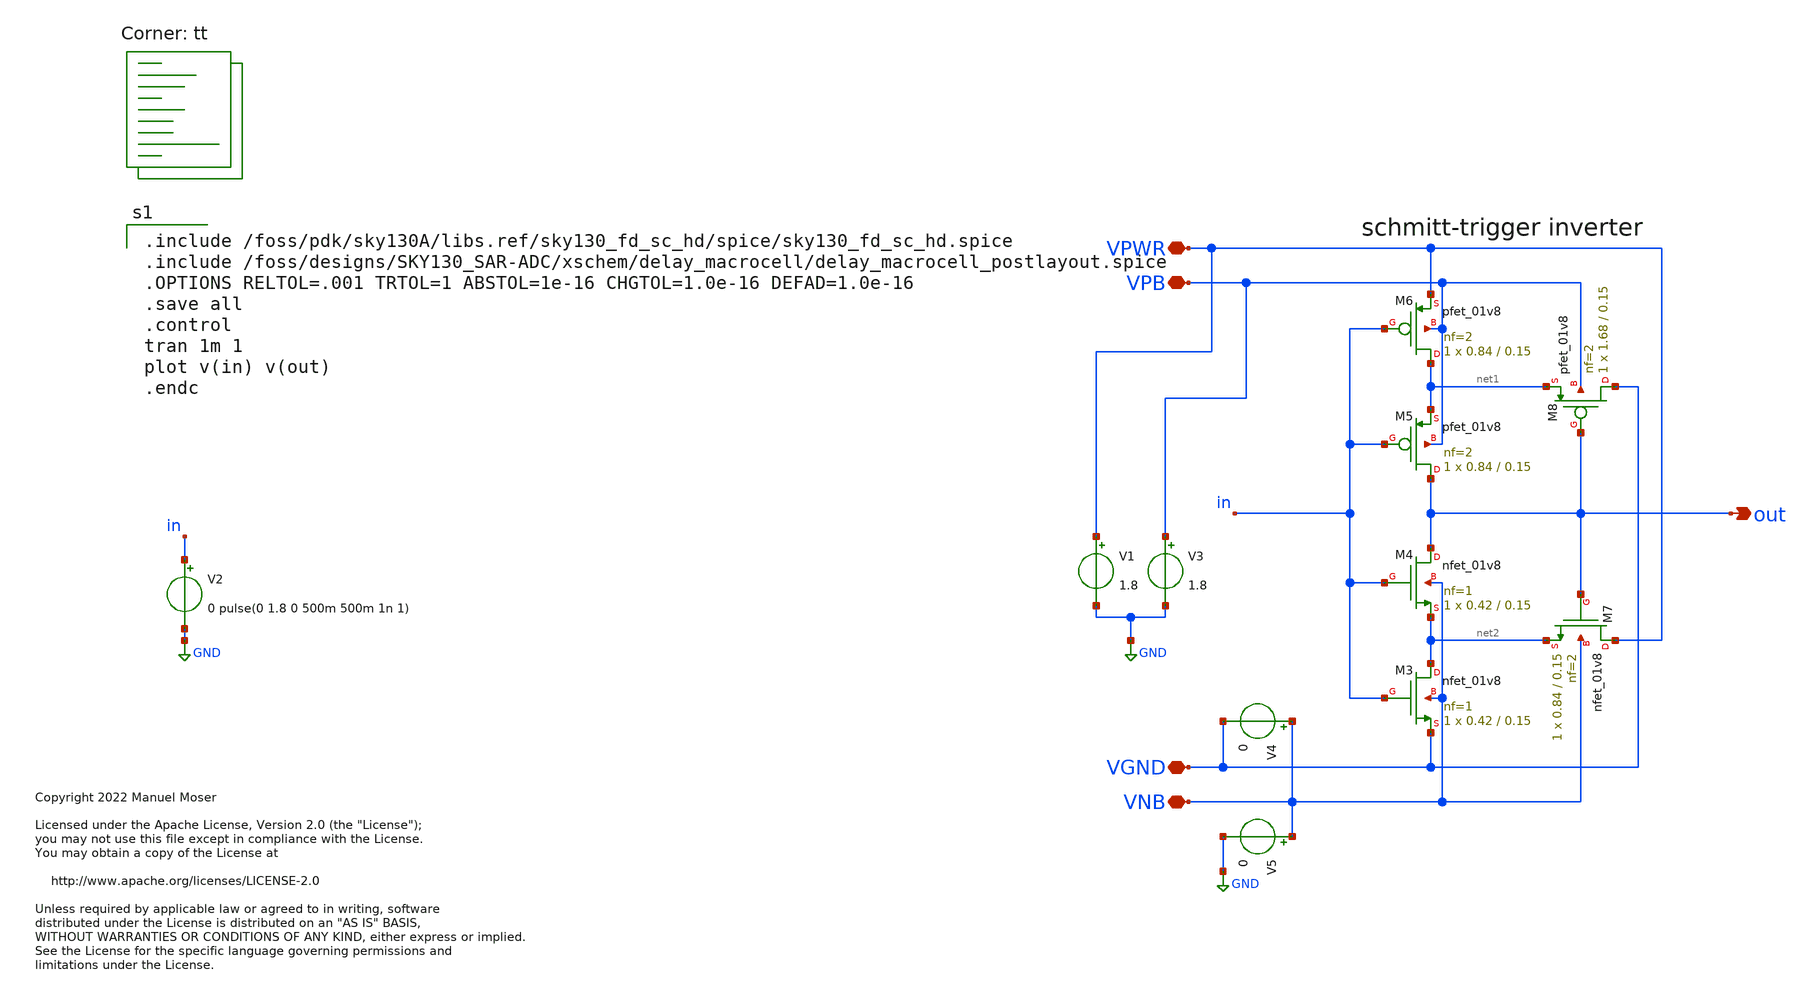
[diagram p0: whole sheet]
** sch_path: xschem/sky130_mm_sc_hd_dly5ns/schmitttrigger.sch
* Copyright 2022 Manuel Moser
* Licensed under the Apache License, Version 2.0 (the "License");
**.subckt schmitttrigger VPWR VGND out VPB VNB
*.iopin VPWR
*.iopin VGND
*.opin out
*.iopin VPB
*.iopin VNB
V1 VPWR GND 1.8
V2 in GND 0 pulse(0 1.8 0 500m 500m 1n 1)
XM3 net2 in VGND VNB sky130_fd_pr__nfet_01v8 L=0.15 W=0.42 nf=1 ad='int((nf+1)/2) * W/nf * 0.29' as='int((nf+2)/2) * W/nf * 0.29'
+ pd='2*int((nf+1)/2) * (W/nf + 0.29)' ps='2*int((nf+2)/2) * (W/nf + 0.29)' nrd='0.29 / W' nrs='0.29 / W'
+ sa=0 sb=0 sd=0 mult=1 m=1
XM4 out in net2 VNB sky130_fd_pr__nfet_01v8 L=0.15 W=0.42 nf=1 ad='int((nf+1)/2) * W/nf * 0.29' as='int((nf+2)/2) * W/nf * 0.29'
+ pd='2*int((nf+1)/2) * (W/nf + 0.29)' ps='2*int((nf+2)/2) * (W/nf + 0.29)' nrd='0.29 / W' nrs='0.29 / W'
+ sa=0 sb=0 sd=0 mult=1 m=1
XM5 out in net1 VPB sky130_fd_pr__pfet_01v8 L=0.15 W=0.84 nf=2 ad='int((nf+1)/2) * W/nf * 0.29' as='int((nf+2)/2) * W/nf * 0.29'
+ pd='2*int((nf+1)/2) * (W/nf + 0.29)' ps='2*int((nf+2)/2) * (W/nf + 0.29)' nrd='0.29 / W' nrs='0.29 / W'
+ sa=0 sb=0 sd=0 mult=1 m=1
XM6 net1 in VPWR VPB sky130_fd_pr__pfet_01v8 L=0.15 W=0.84 nf=2 ad='int((nf+1)/2) * W/nf * 0.29' as='int((nf+2)/2) * W/nf * 0.29'
+ pd='2*int((nf+1)/2) * (W/nf + 0.29)' ps='2*int((nf+2)/2) * (W/nf + 0.29)' nrd='0.29 / W' nrs='0.29 / W'
+ sa=0 sb=0 sd=0 mult=1 m=1
XM7 VPWR out net2 VNB sky130_fd_pr__nfet_01v8 L=0.15 W=0.84 nf=2 ad='int((nf+1)/2) * W/nf * 0.29' as='int((nf+2)/2) * W/nf * 0.29'
+ pd='2*int((nf+1)/2) * (W/nf + 0.29)' ps='2*int((nf+2)/2) * (W/nf + 0.29)' nrd='0.29 / W' nrs='0.29 / W'
+ sa=0 sb=0 sd=0 mult=1 m=1
XM8 VGND out net1 VPB sky130_fd_pr__pfet_01v8 L=0.15 W=1.68 nf=2 ad='int((nf+1)/2) * W/nf * 0.29' as='int((nf+2)/2) * W/nf * 0.29'
+ pd='2*int((nf+1)/2) * (W/nf + 0.29)' ps='2*int((nf+2)/2) * (W/nf + 0.29)' nrd='0.29 / W' nrs='0.29 / W'
+ sa=0 sb=0 sd=0 mult=1 m=1
V3 VPB GND 1.8
V4 VNB VGND 0
V5 VNB GND 0
**** begin user architecture code

.include /foss/pdk/sky130A/libs.ref/sky130_fd_sc_hd/spice/sky130_fd_sc_hd.spice
.include /foss/designs/SKY130_SAR-ADC/xschem/delay_macrocell/delay_macrocell_postlayout.spice
.OPTIONS RELTOL=.001 TRTOL=1 ABSTOL=1e-16 CHGTOL=1.0e-16 DEFAD=1.0e-16
.save all
.control
tran 1m 1
plot v(in) v(out)
.endc

.lib $::SKYWATER_MODELS/sky130.lib.spice tt
**** end user architecture code
**.ends
.GLOBAL GND
.end
